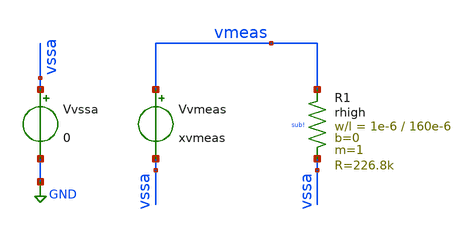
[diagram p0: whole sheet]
** sch_path: tb_res_ihp/tb_res_ihp.sch
**.subckt tb_res_ihp
Vvssa vssa GND 0
Vvmeas vmeas vssa xvmeas
XR1 vmeas vssa sub! rhigh w=1e-6 l=160e-6 m=1 b=0 mm_ok=1
**** begin user architecture code

** opencircuitdesign pdks install
.lib /home/slice/pdk/iHP/IHP-Open-PDK/ihp-sg13g2/libs.tech/ngspice/models/cornerRES.lib res_typ

* Parameters

.param xvmeas = 1
.csparam xvmeas_var = 'xvmeas'
.param xtsim = 5u
.csparam xtsim_var = 'xtsim'
.temp 27

  .save v(vmeas) i(Vvmeas)

  .control

  *set xTj = ( -40 -30 -20 -10 0 10 20 30 40 50 60 70 80 90 100 110 120 130 )
  set xTj = ( 27 )
  foreach xTj_var $xTj

  let Tj_meas = $xTj_var

  echo temperature is "$&Tj_meas"

  set temp = $xTj_var

** 1. TRAN ANALYSIS **

  tran 1n $&xtsim_var
  *set filetype=ascii
  remzerovec
  write tb_res_ihp.raw

** 2. MEASURES **

  meas tran vmeas_avg AVG vmeas
  meas tran imeas_avg AVG i(Vvmeas)
  let rmeas = (vmeas_avg/imeas_avg)*-1
  echo "$&Tj_meas" >> res_measures_T.txt
  echo "$&rmeas"
  echo "$&rmeas" >> res_measures_typ.txt

  end

  setplot
*quit 0
.endc




**** end user architecture code
**.ends
.GLOBAL GND
.end
